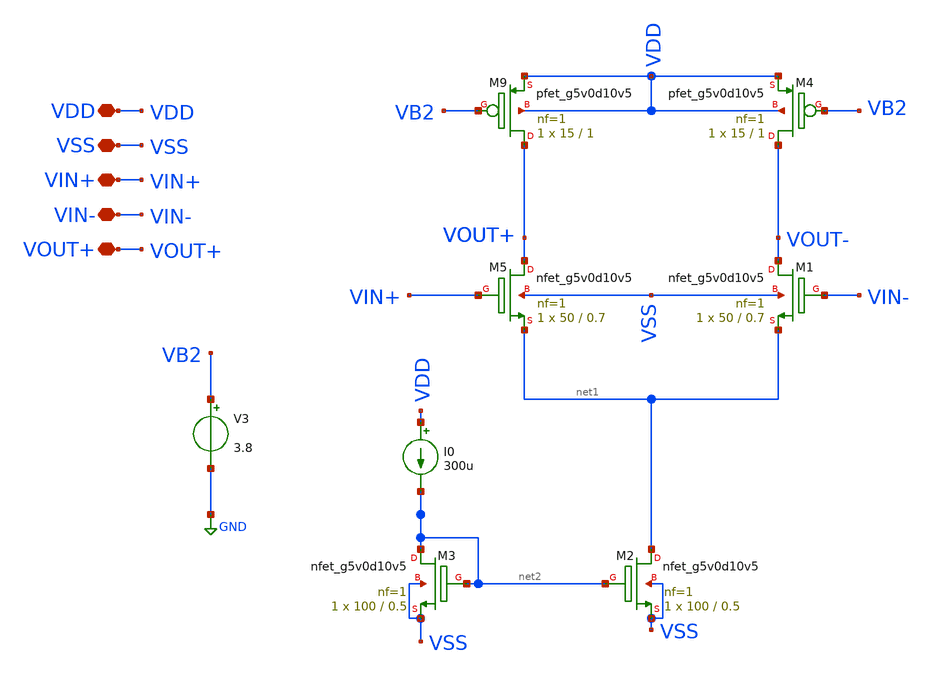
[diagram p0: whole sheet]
** sch_path: old stuff/amplifiers/differencial_stage_amps/basic_stages/basic_NMOS_LOAD_curr_stage/differential_stage.sch
**.subckt differential_stage VDD VSS VIN+ VIN- VOUT+
*.iopin VDD
*.iopin VSS
*.iopin VIN+
*.iopin VIN-
*.iopin VOUT+
XM5 VOUT+ VIN+ net1 VSS sky130_fd_pr__nfet_g5v0d10v5 L=0.7 W=50 nf=1 ad='int((1 + 1)/2) * 50 / 1 * 0.29'
+ as='int((1 + 2)/2) * 50 / 1 * 0.29' pd='2*int((1 + 1)/2) * (50 / 1 + 0.29)' ps='2*int((1 + 2)/2) * (50 / 1 + 0.29)'
+ nrd='0.29 / 50 ' nrs='0.29 / 50 ' sa=0 sb=0 sd=0 mult=1 m=1
XM1 VOUT- VIN- net1 VSS sky130_fd_pr__nfet_g5v0d10v5 L=0.7 W=50 nf=1 ad='int((1 + 1)/2) * 50 / 1 * 0.29'
+ as='int((1 + 2)/2) * 50 / 1 * 0.29' pd='2*int((1 + 1)/2) * (50 / 1 + 0.29)' ps='2*int((1 + 2)/2) * (50 / 1 + 0.29)'
+ nrd='0.29 / 50 ' nrs='0.29 / 50 ' sa=0 sb=0 sd=0 mult=1 m=1
XM2 net1 net2 VSS VSS sky130_fd_pr__nfet_g5v0d10v5 L=0.5 W=100 nf=1 ad='int((1 + 1)/2) * 100 / 1 * 0.29'
+ as='int((1 + 2)/2) * 100 / 1 * 0.29' pd='2*int((1 + 1)/2) * (100 / 1 + 0.29)' ps='2*int((1 + 2)/2) * (100 / 1 + 0.29)'
+ nrd='0.29 / 100 ' nrs='0.29 / 100 ' sa=0 sb=0 sd=0 mult=1 m=1
XM3 net2 net2 VSS VSS sky130_fd_pr__nfet_g5v0d10v5 L=0.5 W=100 nf=1 ad='int((1 + 1)/2) * 100 / 1 * 0.29'
+ as='int((1 + 2)/2) * 100 / 1 * 0.29' pd='2*int((1 + 1)/2) * (100 / 1 + 0.29)' ps='2*int((1 + 2)/2) * (100 / 1 + 0.29)'
+ nrd='0.29 / 100 ' nrs='0.29 / 100 ' sa=0 sb=0 sd=0 mult=1 m=1
I0 VDD net2 300u
XM9 VOUT+ VB2 VDD VDD sky130_fd_pr__pfet_g5v0d10v5 L=1 W=15 nf=1 ad='int((1 + 1)/2) * 15 / 1 * 0.29'
+ as='int((1 + 2)/2) * 15 / 1 * 0.29' pd='2*int((1 + 1)/2) * (15 / 1 + 0.29)' ps='2*int((1 + 2)/2) * (15 / 1 + 0.29)'
+ nrd='0.29 / 15 ' nrs='0.29 / 15 ' sa=0 sb=0 sd=0 mult=1 m=1
XM4 VOUT- VB2 VDD VDD sky130_fd_pr__pfet_g5v0d10v5 L=1 W=15 nf=1 ad='int((1 + 1)/2) * 15 / 1 * 0.29'
+ as='int((1 + 2)/2) * 15 / 1 * 0.29' pd='2*int((1 + 1)/2) * (15 / 1 + 0.29)' ps='2*int((1 + 2)/2) * (15 / 1 + 0.29)'
+ nrd='0.29 / 15 ' nrs='0.29 / 15 ' sa=0 sb=0 sd=0 mult=1 m=1
V3 VB2 GND 3.8
**.ends
.GLOBAL GND
.end
